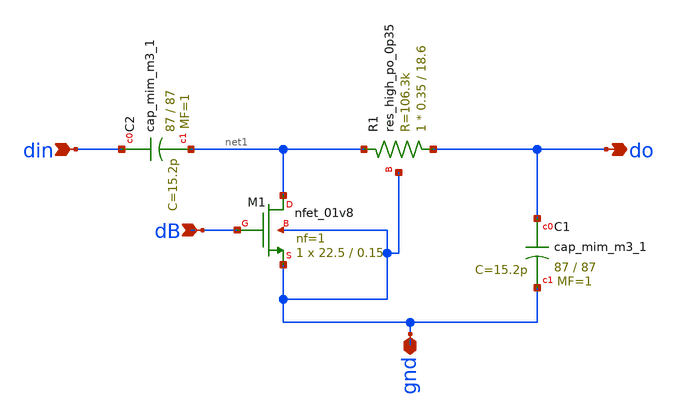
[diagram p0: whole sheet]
** sch_path: xschem/detectorPassivo.sch
**.subckt detectorPassivo din dB do gnd
*.ipin din
*.ipin dB
*.opin do
*.iopin gnd
XM1 net1 dB gnd gnd sky130_fd_pr__nfet_01v8 L=0.15 W=22.5 nf=1 ad='int((nf+1)/2) * W/nf * 0.29' as='int((nf+2)/2) * W/nf * 0.29'
+ pd='2*int((nf+1)/2) * (W/nf + 0.29)' ps='2*int((nf+2)/2) * (W/nf + 0.29)' nrd='0.29 / W' nrs='0.29 / W'
+ sa=0 sb=0 sd=0 mult=1 m=1
XC1 do gnd sky130_fd_pr__cap_mim_m3_1 W=87 L=87 MF=1 m=1
XC2 din net1 sky130_fd_pr__cap_mim_m3_1 W=87 L=87 MF=1 m=1
XR1 do net1 gnd sky130_fd_pr__res_high_po_0p35 L=18.6 mult=1 m=1
**.ends
.end
